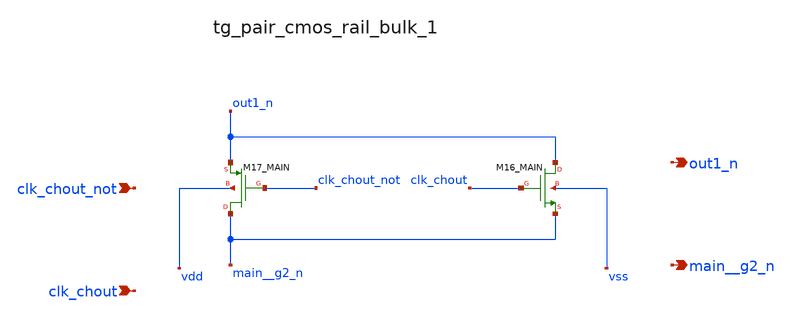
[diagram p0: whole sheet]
** sch_path: analog-db/raw/ia_004_fan_chopper_rrl/hier/blocks/tg_pair_cmos_rail_bulk_1.sch
**.subckt tg_pair_cmos_rail_bulk_1 clk_chout_not clk_chout out1_n main__g2_n
*.ipin clk_chout_not
*.ipin clk_chout
*.opin out1_n
*.opin main__g2_n
XM16_MAIN out1_n clk_chout main__g2_n vss sg13_lv_nmos w=x_dut_xm16_main_w l=x_dut_xm16_main_l ng=1
+ m=x_dut_xm16_main_m
XM17_MAIN main__g2_n clk_chout_not out1_n vdd sg13_lv_pmos w=x_dut_xm17_main_w l=x_dut_xm17_main_l
+ ng=1 m=x_dut_xm17_main_m
**.ends
.end
